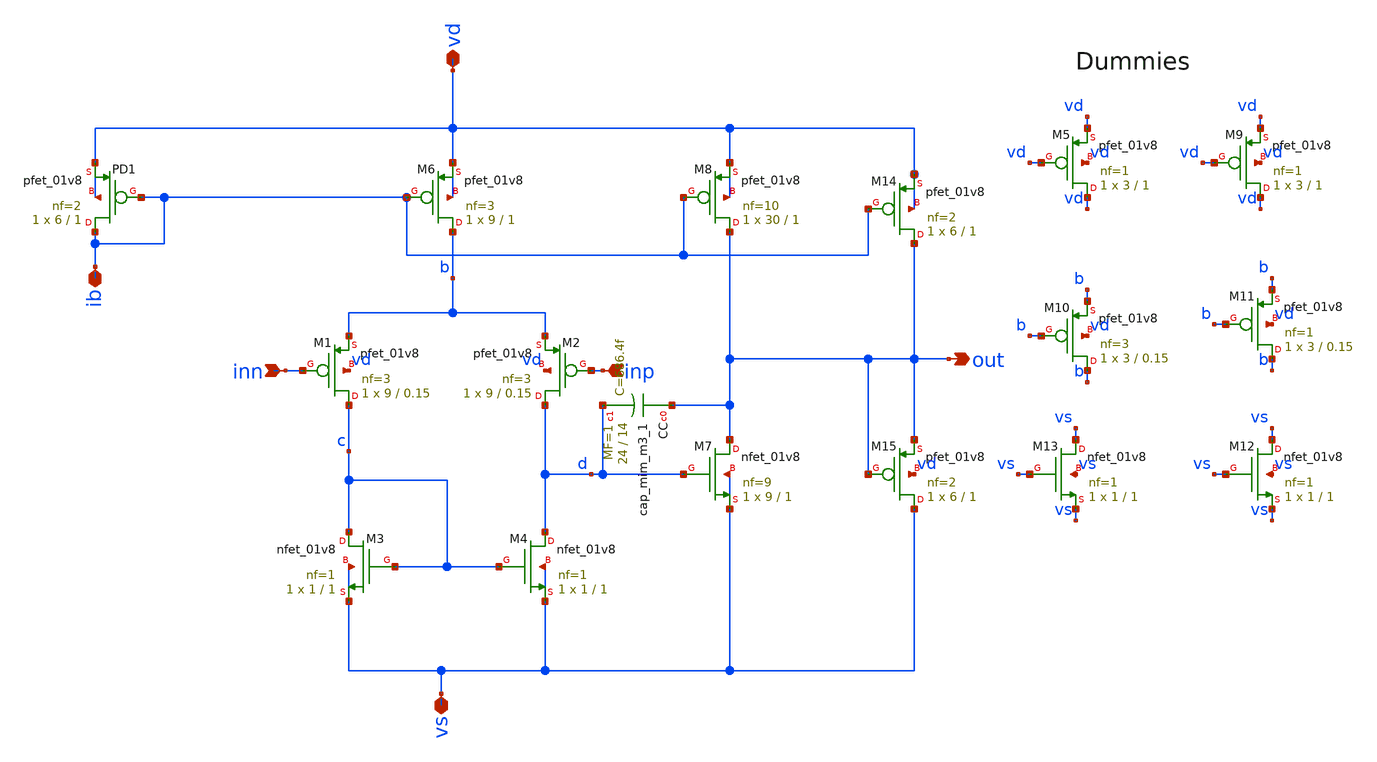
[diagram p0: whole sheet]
** sch_path: ota/xschem/ota.sch
* Copyright 2020 Stefan Frederik Schippers
* Licensed under the Apache License, Version 2.0 (the "License");
* you may not use this file except in compliance with the License.
* You may obtain a copy of the License at
* https://www.apache.org/licenses/LICENSE-2.0
* Unless required by applicable law or agreed to in writing, software
* distributed under the License is distributed on an "AS IS" BASIS,
* WITHOUT WARRANTIES OR CONDITIONS OF ANY KIND, either express or implied.
* See the License for the specific language governing permissions and
* limitations under the License.
**.subckt ota vd vs ib inn inp out
*.iopin vd
*.iopin vs
*.iopin ib
*.ipin inn
*.ipin inp
*.opin out
XCC out d sky130_fd_pr__cap_mim_m3_1 W=24 L=14 MF=1 m=1
XPD1 ib ib vd vd sky130_fd_pr__pfet_01v8 L=1 W=6 nf=2 ad='int((nf+1)/2) * W/nf * 0.29' as='int((nf+2)/2) * W/nf * 0.29'
+ pd='2*int((nf+1)/2) * (W/nf + 0.29)' ps='2*int((nf+2)/2) * (W/nf + 0.29)' nrd='0.29 / W' nrs='0.29 / W'
+ sa=0 sb=0 sd=0 mult=1 m=1
XM6 b ib vd vd sky130_fd_pr__pfet_01v8 L=1 W=9 nf=3 ad='int((nf+1)/2) * W/nf * 0.29' as='int((nf+2)/2) * W/nf * 0.29'
+ pd='2*int((nf+1)/2) * (W/nf + 0.29)' ps='2*int((nf+2)/2) * (W/nf + 0.29)' nrd='0.29 / W' nrs='0.29 / W'
+ sa=0 sb=0 sd=0 mult=1 m=1
XM8 out ib vd vd sky130_fd_pr__pfet_01v8 L=1 W=30 nf=10 ad='int((nf+1)/2) * W/nf * 0.29' as='int((nf+2)/2) * W/nf * 0.29'
+ pd='2*int((nf+1)/2) * (W/nf + 0.29)' ps='2*int((nf+2)/2) * (W/nf + 0.29)' nrd='0.29 / W' nrs='0.29 / W'
+ sa=0 sb=0 sd=0 mult=1 m=1
XM1 c inn b vd sky130_fd_pr__pfet_01v8 L=0.15 W=9 nf=3 ad='int((nf+1)/2) * W/nf * 0.29' as='int((nf+2)/2) * W/nf * 0.29'
+ pd='2*int((nf+1)/2) * (W/nf + 0.29)' ps='2*int((nf+2)/2) * (W/nf + 0.29)' nrd='0.29 / W' nrs='0.29 / W'
+ sa=0 sb=0 sd=0 mult=1 m=1
XM2 d inp b vd sky130_fd_pr__pfet_01v8 L=0.15 W=9 nf=3 ad='int((nf+1)/2) * W/nf * 0.29' as='int((nf+2)/2) * W/nf * 0.29'
+ pd='2*int((nf+1)/2) * (W/nf + 0.29)' ps='2*int((nf+2)/2) * (W/nf + 0.29)' nrd='0.29 / W' nrs='0.29 / W'
+ sa=0 sb=0 sd=0 mult=1 m=1
XM3 c c vs vs sky130_fd_pr__nfet_01v8 L=1 W=1 nf=1 ad='int((nf+1)/2) * W/nf * 0.29' as='int((nf+2)/2) * W/nf * 0.29'
+ pd='2*int((nf+1)/2) * (W/nf + 0.29)' ps='2*int((nf+2)/2) * (W/nf + 0.29)' nrd='0.29 / W' nrs='0.29 / W'
+ sa=0 sb=0 sd=0 mult=1 m=1
XM4 d c vs vs sky130_fd_pr__nfet_01v8 L=1 W=1 nf=1 ad='int((nf+1)/2) * W/nf * 0.29' as='int((nf+2)/2) * W/nf * 0.29'
+ pd='2*int((nf+1)/2) * (W/nf + 0.29)' ps='2*int((nf+2)/2) * (W/nf + 0.29)' nrd='0.29 / W' nrs='0.29 / W'
+ sa=0 sb=0 sd=0 mult=1 m=1
XM7 out d vs vs sky130_fd_pr__nfet_01v8 L=1 W=9 nf=9 ad='int((nf+1)/2) * W/nf * 0.29' as='int((nf+2)/2) * W/nf * 0.29'
+ pd='2*int((nf+1)/2) * (W/nf + 0.29)' ps='2*int((nf+2)/2) * (W/nf + 0.29)' nrd='0.29 / W' nrs='0.29 / W'
+ sa=0 sb=0 sd=0 mult=1 m=1
XM5 vd vd vd vd sky130_fd_pr__pfet_01v8 L=1 W=3 nf=1 ad='int((nf+1)/2) * W/nf * 0.29' as='int((nf+2)/2) * W/nf * 0.29'
+ pd='2*int((nf+1)/2) * (W/nf + 0.29)' ps='2*int((nf+2)/2) * (W/nf + 0.29)' nrd='0.29 / W' nrs='0.29 / W'
+ sa=0 sb=0 sd=0 mult=1 m=1
XM9 vd vd vd vd sky130_fd_pr__pfet_01v8 L=1 W=3 nf=1 ad='int((nf+1)/2) * W/nf * 0.29' as='int((nf+2)/2) * W/nf * 0.29'
+ pd='2*int((nf+1)/2) * (W/nf + 0.29)' ps='2*int((nf+2)/2) * (W/nf + 0.29)' nrd='0.29 / W' nrs='0.29 / W'
+ sa=0 sb=0 sd=0 mult=1 m=1
XM10 b b b vd sky130_fd_pr__pfet_01v8 L=0.15 W=3 nf=3 ad='int((nf+1)/2) * W/nf * 0.29' as='int((nf+2)/2) * W/nf * 0.29'
+ pd='2*int((nf+1)/2) * (W/nf + 0.29)' ps='2*int((nf+2)/2) * (W/nf + 0.29)' nrd='0.29 / W' nrs='0.29 / W'
+ sa=0 sb=0 sd=0 mult=1 m=1
XM11 b b b vd sky130_fd_pr__pfet_01v8 L=0.15 W=3 nf=1 ad='int((nf+1)/2) * W/nf * 0.29' as='int((nf+2)/2) * W/nf * 0.29'
+ pd='2*int((nf+1)/2) * (W/nf + 0.29)' ps='2*int((nf+2)/2) * (W/nf + 0.29)' nrd='0.29 / W' nrs='0.29 / W'
+ sa=0 sb=0 sd=0 mult=1 m=1
XM12 vs vs vs vs sky130_fd_pr__nfet_01v8 L=1 W=1 nf=1 ad='int((nf+1)/2) * W/nf * 0.29' as='int((nf+2)/2) * W/nf * 0.29'
+ pd='2*int((nf+1)/2) * (W/nf + 0.29)' ps='2*int((nf+2)/2) * (W/nf + 0.29)' nrd='0.29 / W' nrs='0.29 / W'
+ sa=0 sb=0 sd=0 mult=1 m=1
XM13 vs vs vs vs sky130_fd_pr__nfet_01v8 L=1 W=1 nf=1 ad='int((nf+1)/2) * W/nf * 0.29' as='int((nf+2)/2) * W/nf * 0.29'
+ pd='2*int((nf+1)/2) * (W/nf + 0.29)' ps='2*int((nf+2)/2) * (W/nf + 0.29)' nrd='0.29 / W' nrs='0.29 / W'
+ sa=0 sb=0 sd=0 mult=1 m=1
XM14 out ib vd vd sky130_fd_pr__pfet_01v8 L=1 W=6 nf=2 ad='int((nf+1)/2) * W/nf * 0.29' as='int((nf+2)/2) * W/nf * 0.29'
+ pd='2*int((nf+1)/2) * (W/nf + 0.29)' ps='2*int((nf+2)/2) * (W/nf + 0.29)' nrd='0.29 / W' nrs='0.29 / W'
+ sa=0 sb=0 sd=0 mult=1 m=1
XM15 vs out out vd sky130_fd_pr__pfet_01v8 L=1 W=6 nf=2 ad='int((nf+1)/2) * W/nf * 0.29' as='int((nf+2)/2) * W/nf * 0.29'
+ pd='2*int((nf+1)/2) * (W/nf + 0.29)' ps='2*int((nf+2)/2) * (W/nf + 0.29)' nrd='0.29 / W' nrs='0.29 / W'
+ sa=0 sb=0 sd=0 mult=1 m=1
**.ends
.end
